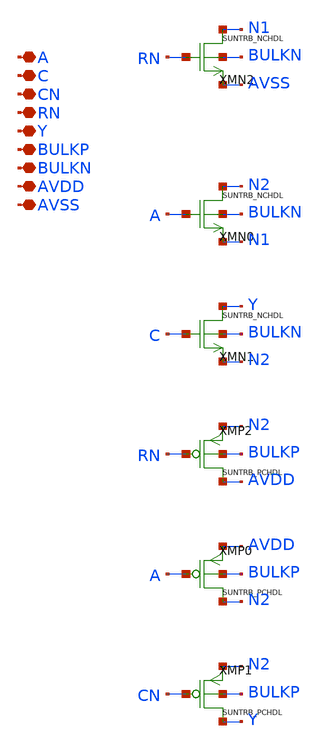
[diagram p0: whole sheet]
** sch_path: design/SUN_TRB_SKY130NM/SUNTRB_NDTRIX1_CV.sch
**.subckt SUNTRB_NDTRIX1_CV A C CN RN Y BULKP BULKN AVDD AVSS
*.iopin A
*.iopin C
*.iopin CN
*.iopin RN
*.iopin Y
*.iopin BULKP
*.iopin BULKN
*.iopin AVDD
*.iopin AVSS
XMN2 N1 RN AVSS BULKN SUNTRB_NCHDL xoffset=0 yoffset=0 angle=0
XMN0 N2 A N1 BULKN SUNTRB_NCHDL xoffset=0 yoffset=0 angle=0
XMN1 Y C N2 BULKN SUNTRB_NCHDL xoffset=0 yoffset=0 angle=0
XMP2 AVDD RN N2 BULKP SUNTRB_PCHDL xoffset=0 yoffset=0 angle=0 M=1
XMP0 N2 A AVDD BULKP SUNTRB_PCHDL xoffset=0 yoffset=0 angle=0 M=1
XMP1 Y CN N2 BULKP SUNTRB_PCHDL xoffset=0 yoffset=0 angle=0 M=1
**.ends
.end
